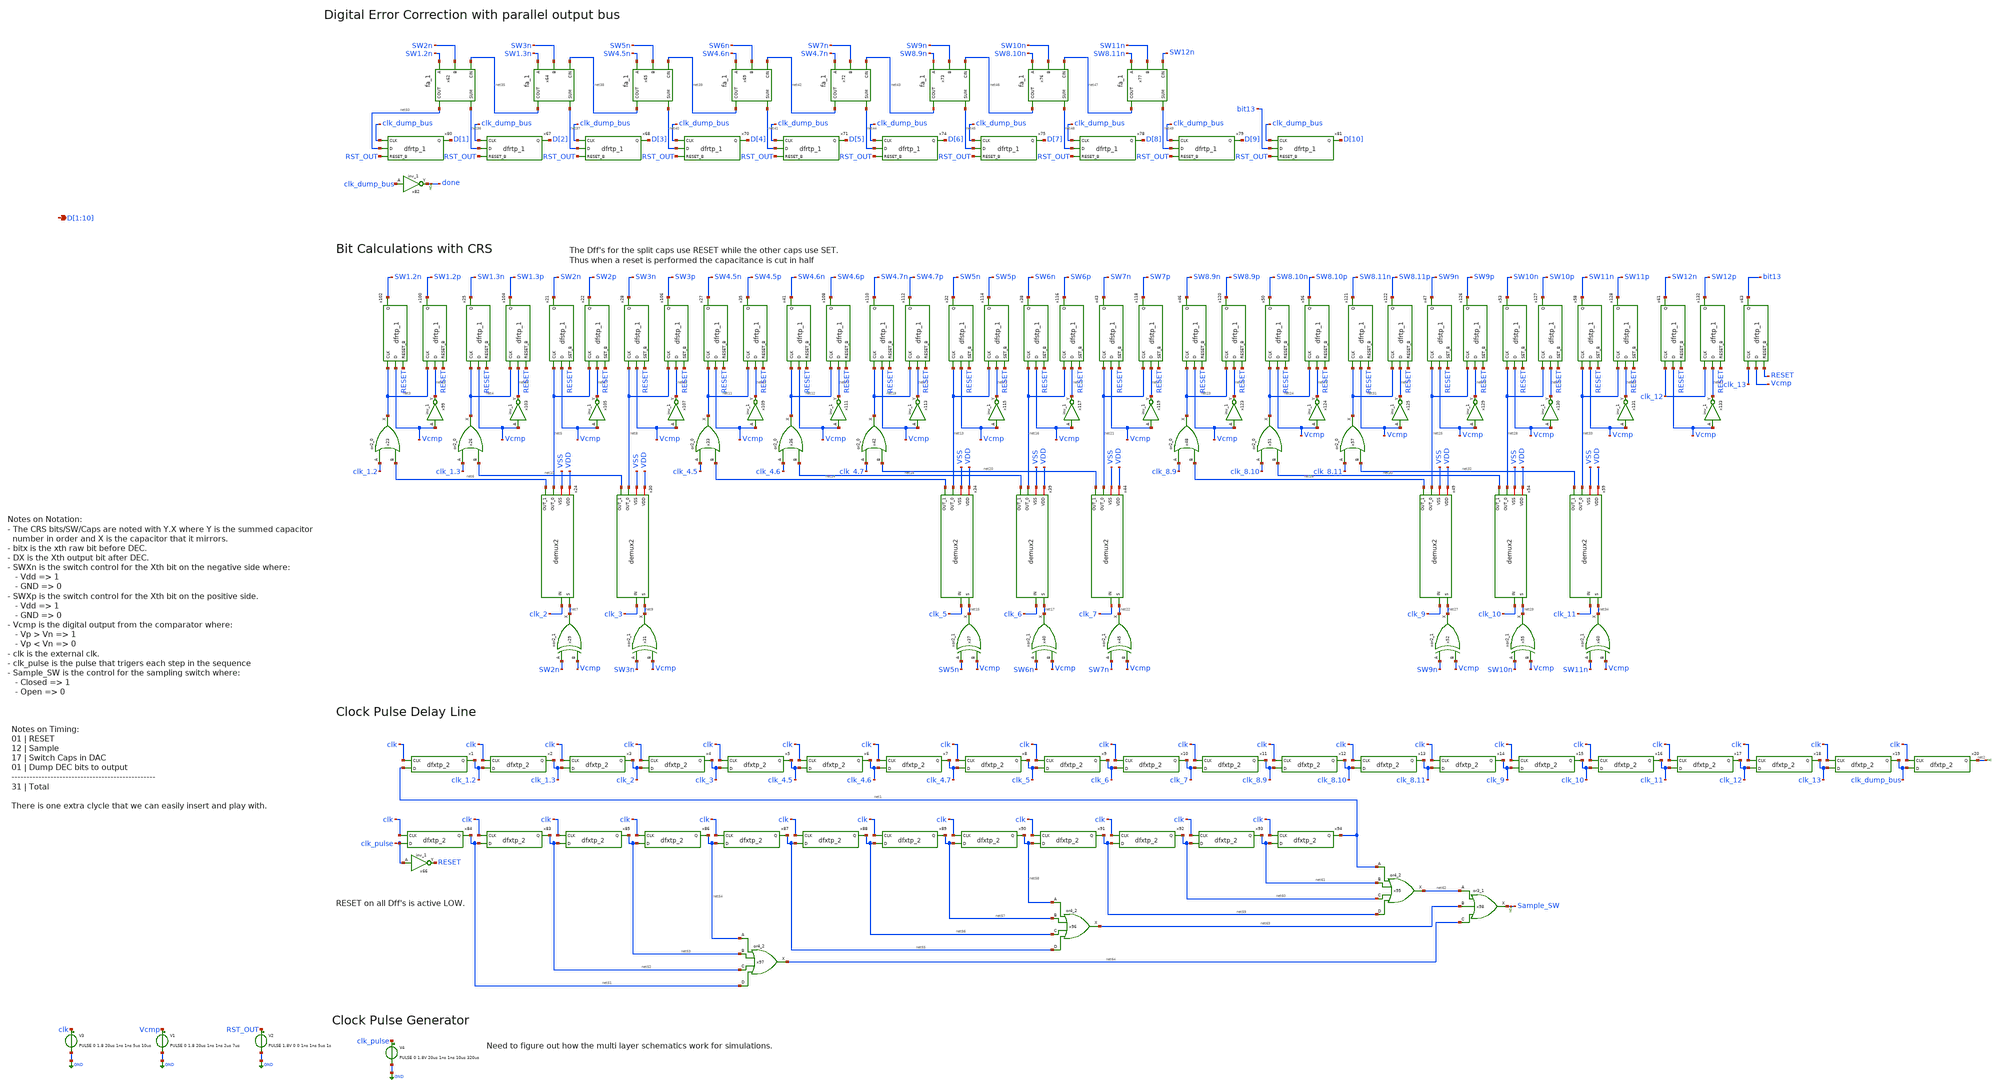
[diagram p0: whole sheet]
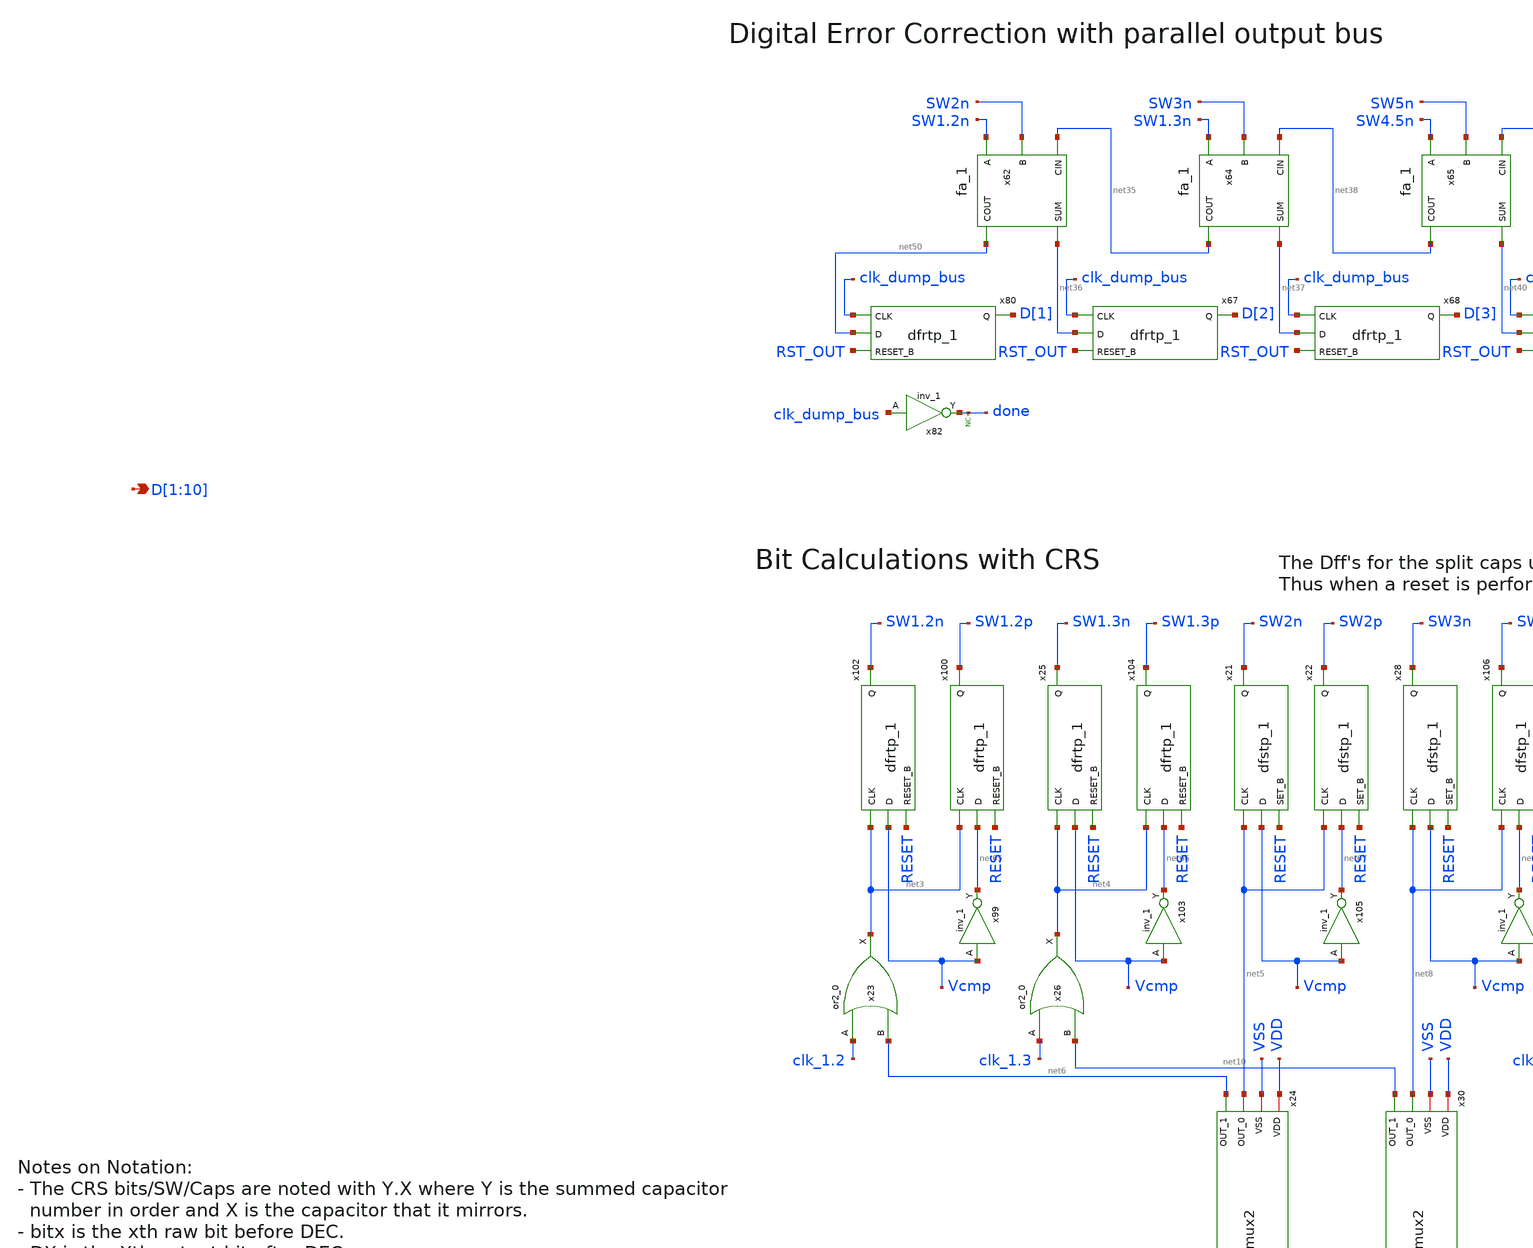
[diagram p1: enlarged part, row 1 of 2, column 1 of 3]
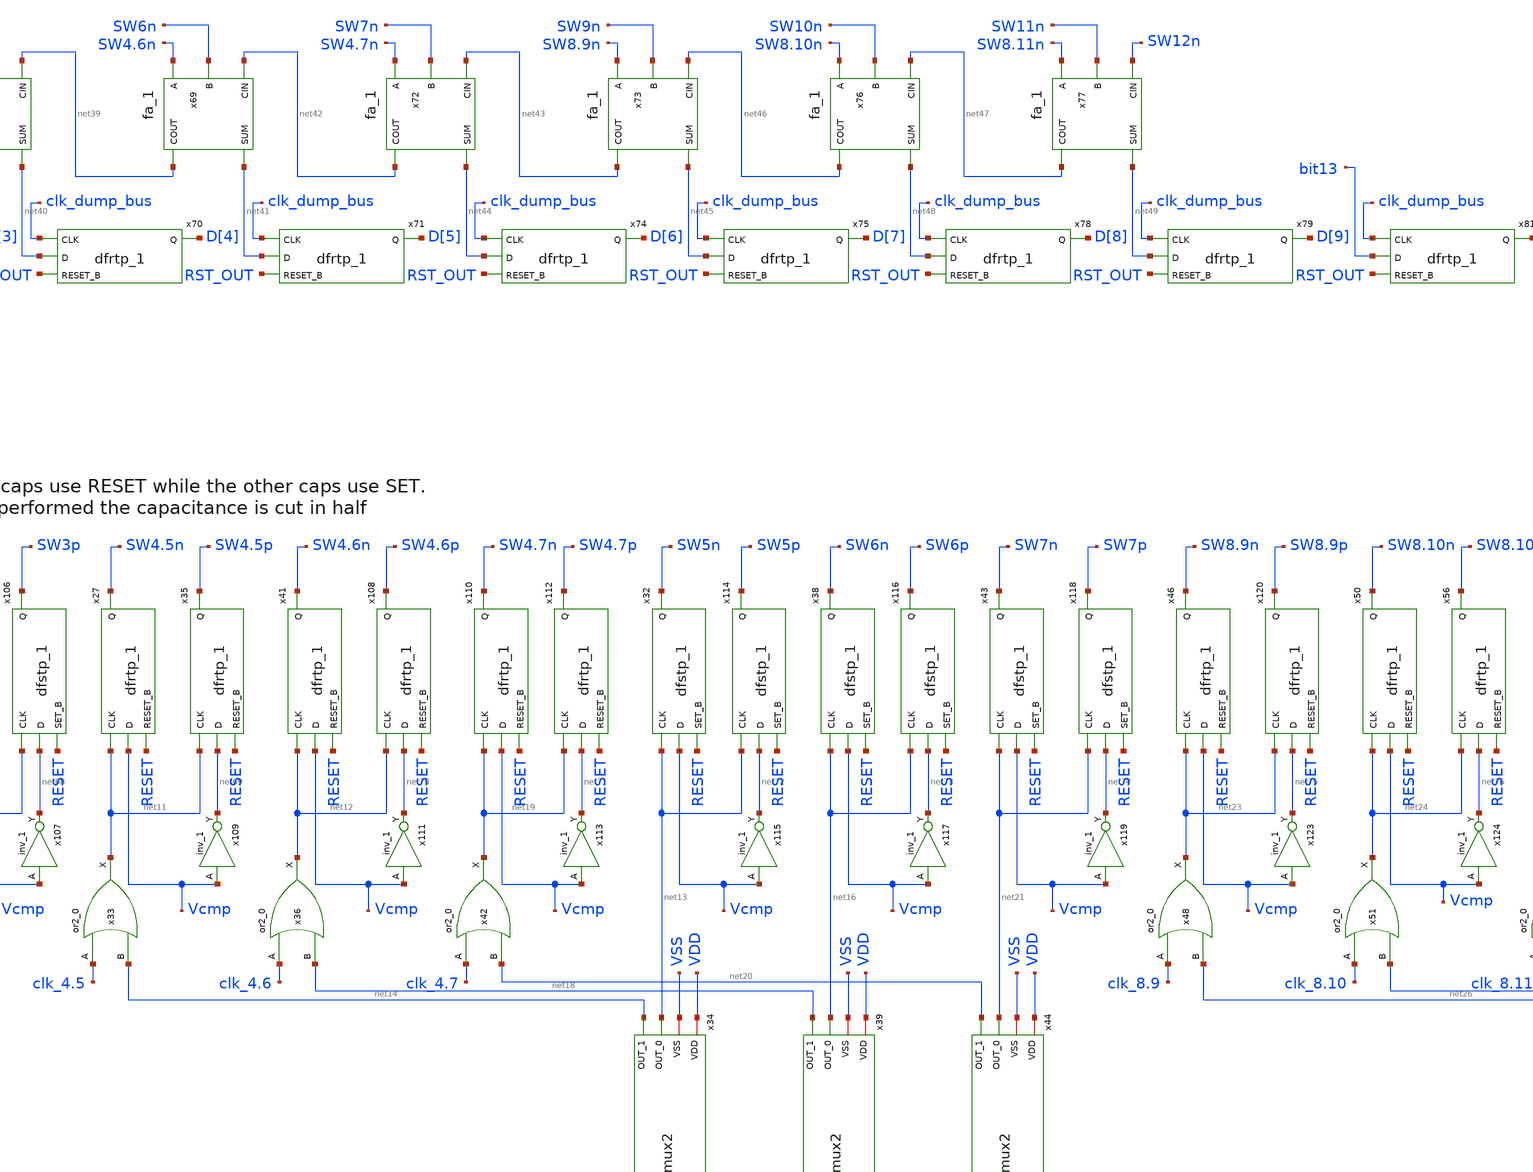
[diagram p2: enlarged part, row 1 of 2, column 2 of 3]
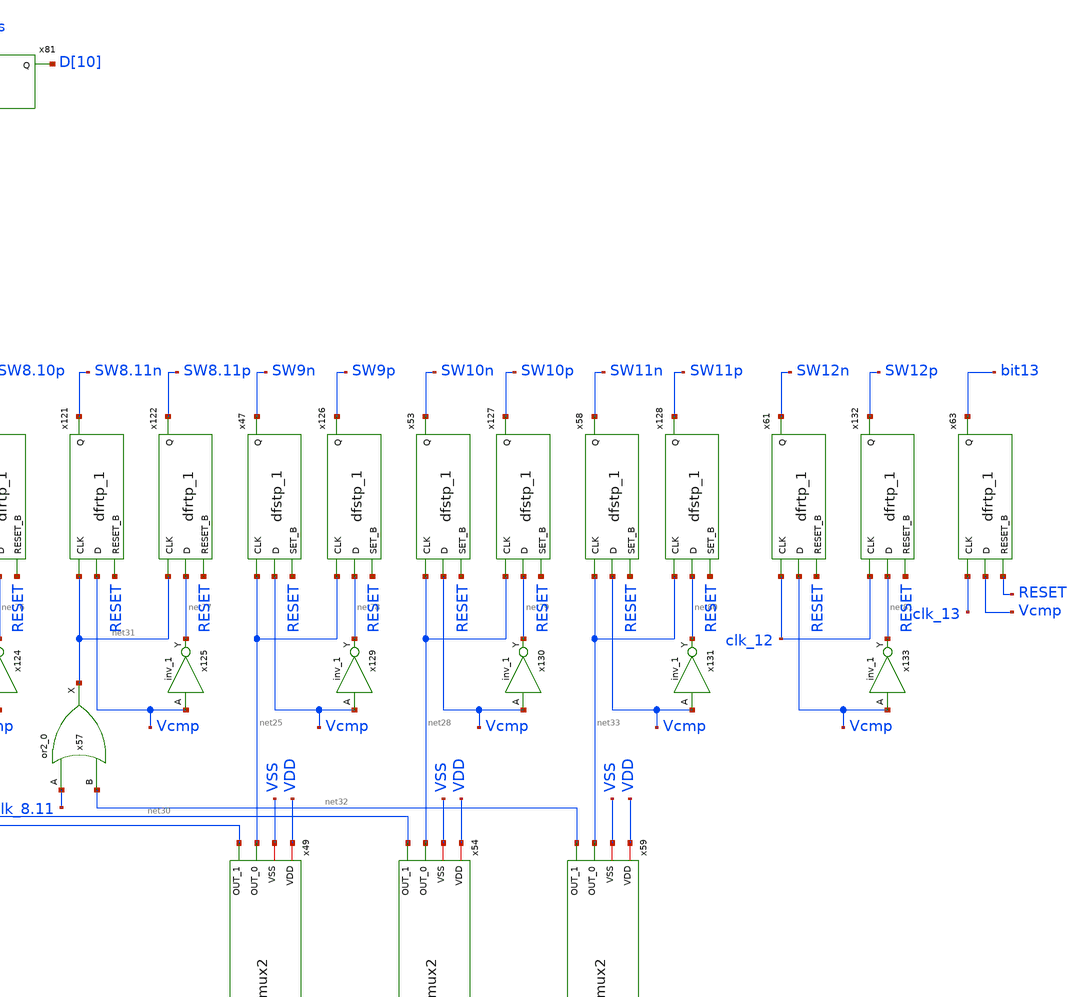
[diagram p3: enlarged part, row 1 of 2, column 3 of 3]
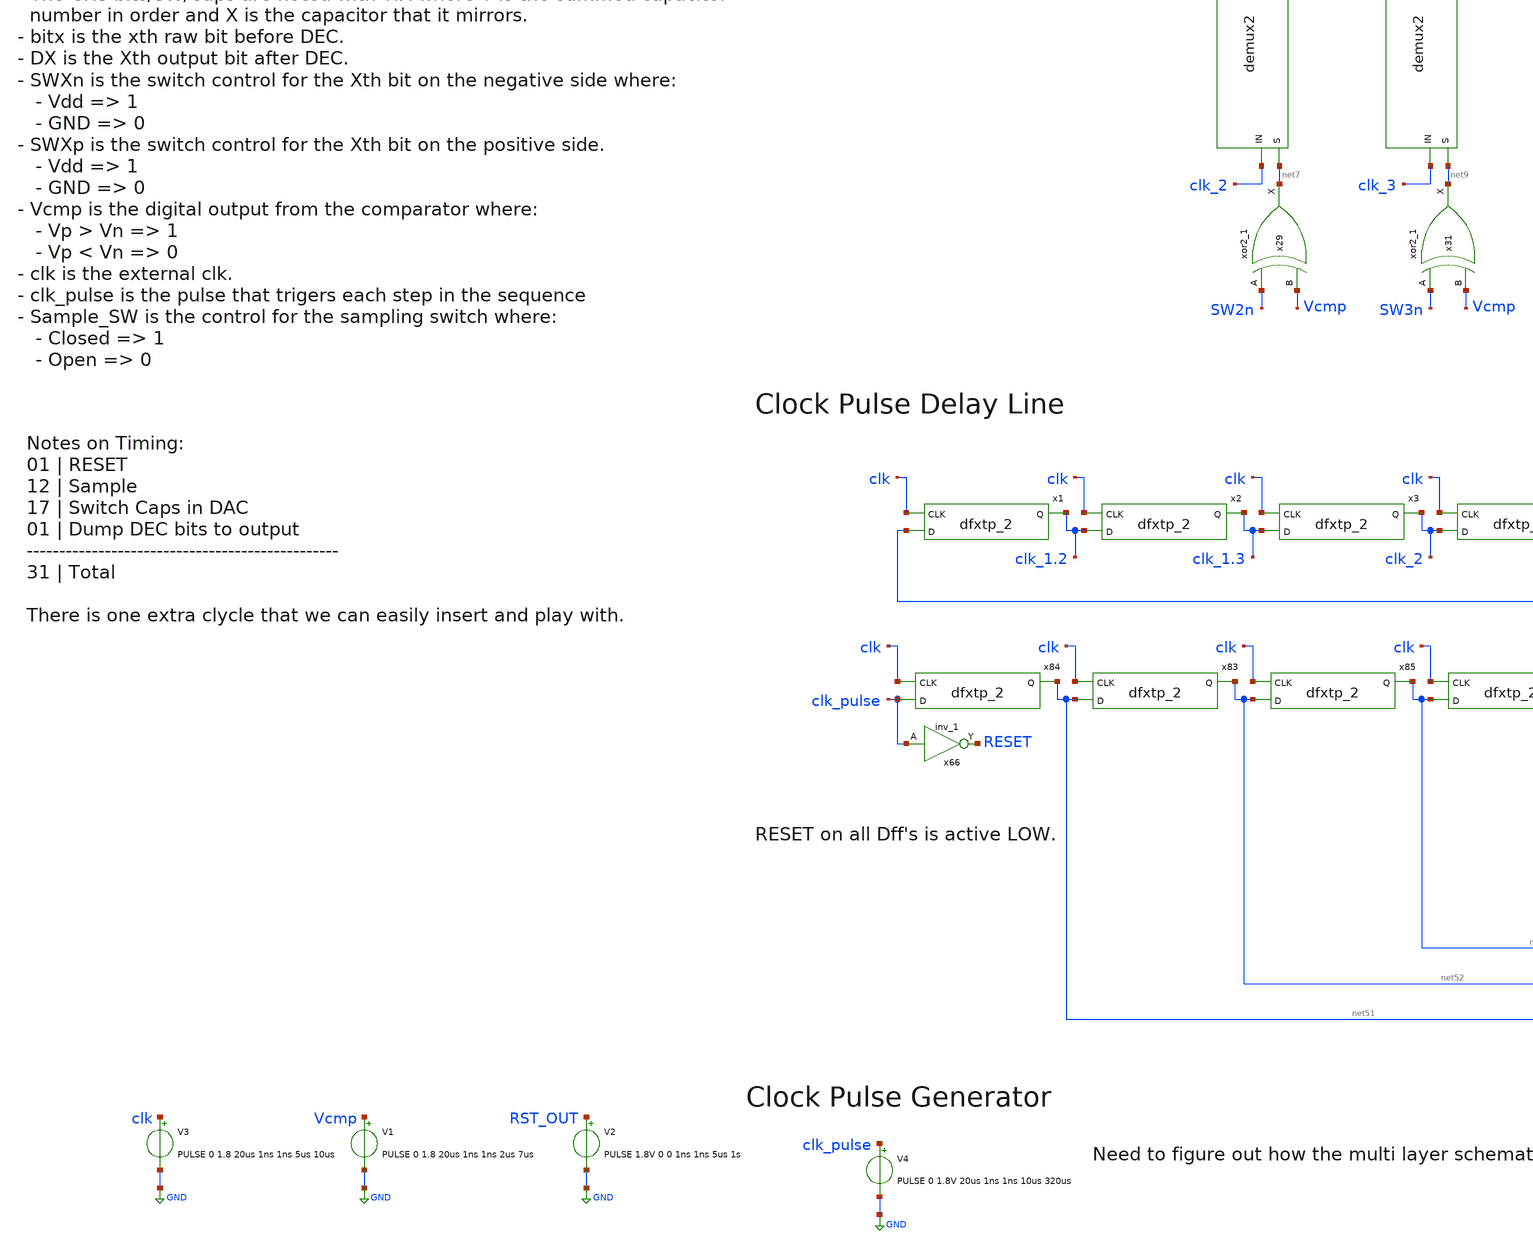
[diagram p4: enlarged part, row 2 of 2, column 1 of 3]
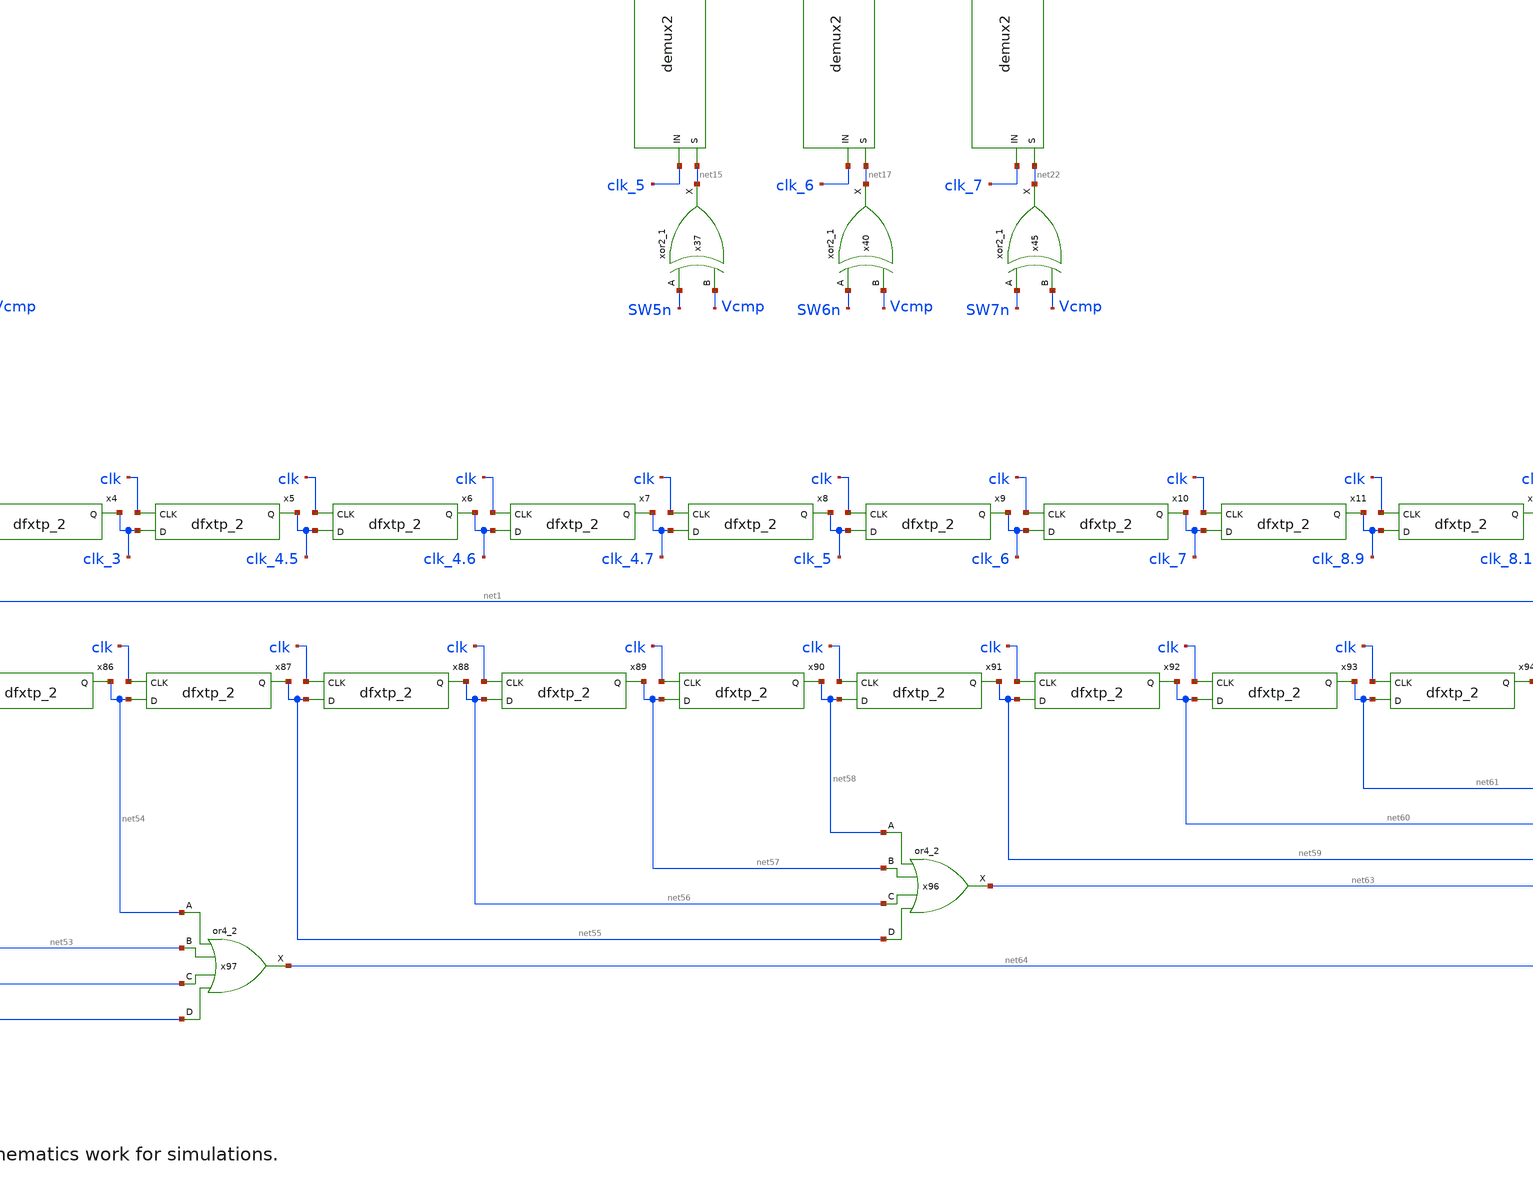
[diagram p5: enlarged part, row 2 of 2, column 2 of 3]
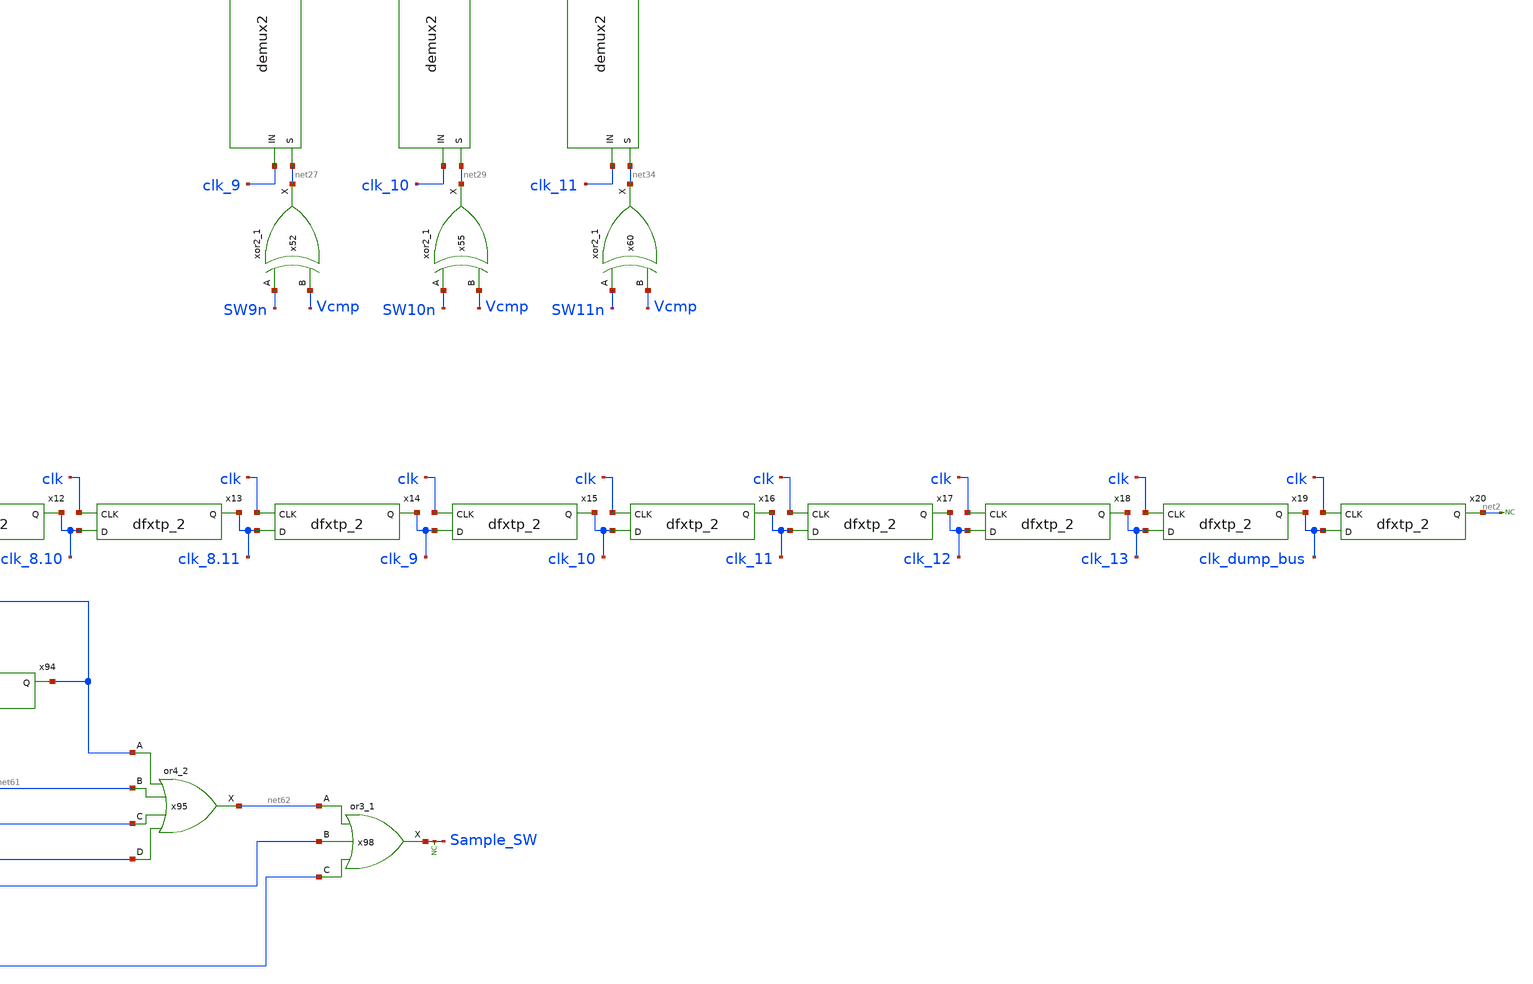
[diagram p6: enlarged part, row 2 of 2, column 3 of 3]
** sch_path: xschem/src/controller/controller.sch
**.subckt controller D[1],D[2],D[3],D[4],D[5],D[6],D[7],D[8],D[9],D[10]
*.opin D[1],D[2],D[3],D[4],D[5],D[6],D[7],D[8],D[9],D[10]
x2 clk clk_1.2 VSS VSS VDD VDD clk_1.3 sky130_fd_sc_hd__dfxtp_2
x1 clk net1 VSS VSS VDD VDD clk_1.2 sky130_fd_sc_hd__dfxtp_2
x3 clk clk_1.3 VSS VSS VDD VDD clk_2 sky130_fd_sc_hd__dfxtp_2
x4 clk clk_2 VSS VSS VDD VDD clk_3 sky130_fd_sc_hd__dfxtp_2
x5 clk clk_3 VSS VSS VDD VDD clk_4.5 sky130_fd_sc_hd__dfxtp_2
x6 clk clk_4.5 VSS VSS VDD VDD clk_4.6 sky130_fd_sc_hd__dfxtp_2
x7 clk clk_4.6 VSS VSS VDD VDD clk_4.7 sky130_fd_sc_hd__dfxtp_2
x8 clk clk_4.7 VSS VSS VDD VDD clk_5 sky130_fd_sc_hd__dfxtp_2
x9 clk clk_5 VSS VSS VDD VDD clk_6 sky130_fd_sc_hd__dfxtp_2
x10 clk clk_6 VSS VSS VDD VDD clk_7 sky130_fd_sc_hd__dfxtp_2
x11 clk clk_7 VSS VSS VDD VDD clk_8.9 sky130_fd_sc_hd__dfxtp_2
x12 clk clk_8.9 VSS VSS VDD VDD clk_8.10 sky130_fd_sc_hd__dfxtp_2
x13 clk clk_8.10 VSS VSS VDD VDD clk_8.11 sky130_fd_sc_hd__dfxtp_2
x14 clk clk_8.11 VSS VSS VDD VDD clk_9 sky130_fd_sc_hd__dfxtp_2
x15 clk clk_9 VSS VSS VDD VDD clk_10 sky130_fd_sc_hd__dfxtp_2
x16 clk clk_10 VSS VSS VDD VDD clk_11 sky130_fd_sc_hd__dfxtp_2
x17 clk clk_11 VSS VSS VDD VDD clk_12 sky130_fd_sc_hd__dfxtp_2
x18 clk clk_12 VSS VSS VDD VDD clk_13 sky130_fd_sc_hd__dfxtp_2
x19 clk clk_13 VSS VSS VDD VDD clk_dump_bus sky130_fd_sc_hd__dfxtp_2
x20 clk clk_dump_bus VSS VSS VDD VDD net2 sky130_fd_sc_hd__dfxtp_2
x23 clk_1.2 net6 VSS VSS VDD VDD net3 sky130_fd_sc_hd__or2_0
x26 clk_1.3 net10 VSS VSS VDD VDD net4 sky130_fd_sc_hd__or2_0
x29 SW2n Vcmp VSS VSS VDD VDD net7 sky130_fd_sc_hd__xor2_1
x31 SW3n Vcmp VSS VSS VDD VDD net9 sky130_fd_sc_hd__xor2_1
x33 clk_4.5 net14 VSS VSS VDD VDD net11 sky130_fd_sc_hd__or2_0
x36 clk_4.6 net18 VSS VSS VDD VDD net12 sky130_fd_sc_hd__or2_0
x37 SW5n Vcmp VSS VSS VDD VDD net15 sky130_fd_sc_hd__xor2_1
x40 SW6n Vcmp VSS VSS VDD VDD net17 sky130_fd_sc_hd__xor2_1
x42 clk_4.7 net20 VSS VSS VDD VDD net19 sky130_fd_sc_hd__or2_0
x45 SW7n Vcmp VSS VSS VDD VDD net22 sky130_fd_sc_hd__xor2_1
x48 clk_8.9 net26 VSS VSS VDD VDD net23 sky130_fd_sc_hd__or2_0
x51 clk_8.10 net30 VSS VSS VDD VDD net24 sky130_fd_sc_hd__or2_0
x52 SW9n Vcmp VSS VSS VDD VDD net27 sky130_fd_sc_hd__xor2_1
x55 SW10n Vcmp VSS VSS VDD VDD net29 sky130_fd_sc_hd__xor2_1
x57 clk_8.11 net32 VSS VSS VDD VDD net31 sky130_fd_sc_hd__or2_0
x60 SW11n Vcmp VSS VSS VDD VDD net34 sky130_fd_sc_hd__xor2_1
x63 clk_13 Vcmp RESET VSS VSS VDD VDD bit13 sky130_fd_sc_hd__dfrtp_1
x62 SW1.2n SW2n net35 VSS VSS VDD VDD net50 net36 sky130_fd_sc_hd__fa_1
x64 SW1.3n SW3n net38 VSS VSS VDD VDD net35 net37 sky130_fd_sc_hd__fa_1
x67 clk_dump_bus net36 RST_OUT VSS VSS VDD VDD D[2] sky130_fd_sc_hd__dfrtp_1
x68 clk_dump_bus net37 RST_OUT VSS VSS VDD VDD D[3] sky130_fd_sc_hd__dfrtp_1
x65 SW4.5n SW5n net39 VSS VSS VDD VDD net38 net40 sky130_fd_sc_hd__fa_1
x69 SW4.6n SW6n net42 VSS VSS VDD VDD net39 net41 sky130_fd_sc_hd__fa_1
x70 clk_dump_bus net40 RST_OUT VSS VSS VDD VDD D[4] sky130_fd_sc_hd__dfrtp_1
x71 clk_dump_bus net41 RST_OUT VSS VSS VDD VDD D[5] sky130_fd_sc_hd__dfrtp_1
x72 SW4.7n SW7n net43 VSS VSS VDD VDD net42 net44 sky130_fd_sc_hd__fa_1
x73 SW8.9n SW9n net46 VSS VSS VDD VDD net43 net45 sky130_fd_sc_hd__fa_1
x74 clk_dump_bus net44 RST_OUT VSS VSS VDD VDD D[6] sky130_fd_sc_hd__dfrtp_1
x75 clk_dump_bus net45 RST_OUT VSS VSS VDD VDD D[7] sky130_fd_sc_hd__dfrtp_1
x76 SW8.10n SW10n net47 VSS VSS VDD VDD net46 net48 sky130_fd_sc_hd__fa_1
x77 SW8.11n SW11n SW12n VSS VSS VDD VDD net47 net49 sky130_fd_sc_hd__fa_1
x78 clk_dump_bus net48 RST_OUT VSS VSS VDD VDD D[8] sky130_fd_sc_hd__dfrtp_1
x79 clk_dump_bus net49 RST_OUT VSS VSS VDD VDD D[9] sky130_fd_sc_hd__dfrtp_1
x80 clk_dump_bus net50 RST_OUT VSS VSS VDD VDD D[1] sky130_fd_sc_hd__dfrtp_1
x81 clk_dump_bus bit13 RST_OUT VSS VSS VDD VDD D[10] sky130_fd_sc_hd__dfrtp_1
x82 clk_dump_bus VSS VSS VDD VDD done sky130_fd_sc_hd__inv_1
x83 clk net51 VSS VSS VDD VDD net52 sky130_fd_sc_hd__dfxtp_2
x84 clk clk_pulse VSS VSS VDD VDD net51 sky130_fd_sc_hd__dfxtp_2
x85 clk net52 VSS VSS VDD VDD net53 sky130_fd_sc_hd__dfxtp_2
x86 clk net53 VSS VSS VDD VDD net54 sky130_fd_sc_hd__dfxtp_2
x87 clk net54 VSS VSS VDD VDD net55 sky130_fd_sc_hd__dfxtp_2
x88 clk net55 VSS VSS VDD VDD net56 sky130_fd_sc_hd__dfxtp_2
x89 clk net56 VSS VSS VDD VDD net57 sky130_fd_sc_hd__dfxtp_2
x90 clk net57 VSS VSS VDD VDD net58 sky130_fd_sc_hd__dfxtp_2
x91 clk net58 VSS VSS VDD VDD net59 sky130_fd_sc_hd__dfxtp_2
x92 clk net59 VSS VSS VDD VDD net60 sky130_fd_sc_hd__dfxtp_2
x93 clk net60 VSS VSS VDD VDD net61 sky130_fd_sc_hd__dfxtp_2
x94 clk net61 VSS VSS VDD VDD net1 sky130_fd_sc_hd__dfxtp_2
x66 clk_pulse VSS VSS VDD VDD RESET sky130_fd_sc_hd__inv_1
x95 net1 net61 net60 net59 VSS VSS VDD VDD net62 sky130_fd_sc_hd__or4_2
x96 net58 net57 net56 net55 VSS VSS VDD VDD net63 sky130_fd_sc_hd__or4_2
x97 net54 net53 net52 net51 VSS VSS VDD VDD net64 sky130_fd_sc_hd__or4_2
x98 net62 net63 net64 VSS VSS VDD VDD Sample_SW sky130_fd_sc_hd__or3_1
V1 Vcmp GND PULSE 0 1.8 20us 1ns 1ns 2us 7us
V2 RST_OUT GND PULSE 1.8V 0 0 1ns 1ns 5us 1s
* noconn #net2
* noconn Sample_SW
* noconn done
V3 clk GND PULSE 0 1.8 20us 1ns 1ns 5us 10us
V4 clk_pulse GND PULSE 0 1.8V 20us 1ns 1ns 10us 320us
x100 net3 net65 RESET VSS VSS VDD VDD SW1.2p sky130_fd_sc_hd__dfrtp_1
x99 Vcmp VSS VSS VDD VDD net65 sky130_fd_sc_hd__inv_1
x102 net3 Vcmp RESET VSS VSS VDD VDD SW1.2n sky130_fd_sc_hd__dfrtp_1
x25 net4 Vcmp RESET VSS VSS VDD VDD SW1.3n sky130_fd_sc_hd__dfrtp_1
x103 Vcmp VSS VSS VDD VDD net66 sky130_fd_sc_hd__inv_1
x104 net4 net66 RESET VSS VSS VDD VDD SW1.3p sky130_fd_sc_hd__dfrtp_1
x21 net5 Vcmp RESET VSS VSS VDD VDD SW2n sky130_fd_sc_hd__dfstp_1
x22 net5 net67 RESET VSS VSS VDD VDD SW2p sky130_fd_sc_hd__dfstp_1
x105 Vcmp VSS VSS VDD VDD net67 sky130_fd_sc_hd__inv_1
x28 net8 Vcmp RESET VSS VSS VDD VDD SW3n sky130_fd_sc_hd__dfstp_1
x106 net8 net68 RESET VSS VSS VDD VDD SW3p sky130_fd_sc_hd__dfstp_1
x107 Vcmp VSS VSS VDD VDD net68 sky130_fd_sc_hd__inv_1
x109 Vcmp VSS VSS VDD VDD net69 sky130_fd_sc_hd__inv_1
x111 Vcmp VSS VSS VDD VDD net70 sky130_fd_sc_hd__inv_1
x27 net11 Vcmp RESET VSS VSS VDD VDD SW4.5n sky130_fd_sc_hd__dfrtp_1
x35 net11 net69 RESET VSS VSS VDD VDD SW4.5p sky130_fd_sc_hd__dfrtp_1
x41 net12 Vcmp RESET VSS VSS VDD VDD SW4.6n sky130_fd_sc_hd__dfrtp_1
x108 net12 net70 RESET VSS VSS VDD VDD SW4.6p sky130_fd_sc_hd__dfrtp_1
x110 net19 Vcmp RESET VSS VSS VDD VDD SW4.7n sky130_fd_sc_hd__dfrtp_1
x112 net19 net71 RESET VSS VSS VDD VDD SW4.7p sky130_fd_sc_hd__dfrtp_1
x113 Vcmp VSS VSS VDD VDD net71 sky130_fd_sc_hd__inv_1
x114 net13 net72 RESET VSS VSS VDD VDD SW5p sky130_fd_sc_hd__dfstp_1
x32 net13 Vcmp RESET VSS VSS VDD VDD SW5n sky130_fd_sc_hd__dfstp_1
x115 Vcmp VSS VSS VDD VDD net72 sky130_fd_sc_hd__inv_1
x38 net16 Vcmp RESET VSS VSS VDD VDD SW6n sky130_fd_sc_hd__dfstp_1
x116 net16 net73 RESET VSS VSS VDD VDD SW6p sky130_fd_sc_hd__dfstp_1
x117 Vcmp VSS VSS VDD VDD net73 sky130_fd_sc_hd__inv_1
x43 net21 Vcmp RESET VSS VSS VDD VDD SW7n sky130_fd_sc_hd__dfstp_1
x118 net21 net74 RESET VSS VSS VDD VDD SW7p sky130_fd_sc_hd__dfstp_1
x119 Vcmp VSS VSS VDD VDD net74 sky130_fd_sc_hd__inv_1
x120 net23 net75 RESET VSS VSS VDD VDD SW8.9p sky130_fd_sc_hd__dfrtp_1
x46 net23 Vcmp RESET VSS VSS VDD VDD SW8.9n sky130_fd_sc_hd__dfrtp_1
x50 net24 Vcmp RESET VSS VSS VDD VDD SW8.10n sky130_fd_sc_hd__dfrtp_1
x56 net24 net76 RESET VSS VSS VDD VDD SW8.10p sky130_fd_sc_hd__dfrtp_1
x121 net31 Vcmp RESET VSS VSS VDD VDD SW8.11n sky130_fd_sc_hd__dfrtp_1
x122 net31 net77 RESET VSS VSS VDD VDD SW8.11p sky130_fd_sc_hd__dfrtp_1
x123 Vcmp VSS VSS VDD VDD net75 sky130_fd_sc_hd__inv_1
x124 Vcmp VSS VSS VDD VDD net76 sky130_fd_sc_hd__inv_1
x125 Vcmp VSS VSS VDD VDD net77 sky130_fd_sc_hd__inv_1
x126 net25 net78 RESET VSS VSS VDD VDD SW9p sky130_fd_sc_hd__dfstp_1
x47 net25 Vcmp RESET VSS VSS VDD VDD SW9n sky130_fd_sc_hd__dfstp_1
x53 net28 Vcmp RESET VSS VSS VDD VDD SW10n sky130_fd_sc_hd__dfstp_1
x58 net33 Vcmp RESET VSS VSS VDD VDD SW11n sky130_fd_sc_hd__dfstp_1
x127 net28 net79 RESET VSS VSS VDD VDD SW10p sky130_fd_sc_hd__dfstp_1
x128 net33 net80 RESET VSS VSS VDD VDD SW11p sky130_fd_sc_hd__dfstp_1
x129 Vcmp VSS VSS VDD VDD net78 sky130_fd_sc_hd__inv_1
x130 Vcmp VSS VSS VDD VDD net79 sky130_fd_sc_hd__inv_1
x131 Vcmp VSS VSS VDD VDD net80 sky130_fd_sc_hd__inv_1
x132 clk_12 net81 RESET VSS VSS VDD VDD SW12p sky130_fd_sc_hd__dfrtp_1
x133 Vcmp VSS VSS VDD VDD net81 sky130_fd_sc_hd__inv_1
x61 clk_12 Vcmp RESET VSS VSS VDD VDD SW12n sky130_fd_sc_hd__dfrtp_1
x24 net7 VDD VSS net5 clk_2 net6 demux2
x30 net9 VDD VSS net8 clk_3 net10 demux2
x34 net15 VDD VSS net13 clk_5 net14 demux2
x39 net17 VDD VSS net16 clk_6 net18 demux2
x44 net22 VDD VSS net21 clk_7 net20 demux2
x49 net27 VDD VSS net25 clk_9 net26 demux2
x54 net29 VDD VSS net28 clk_10 net30 demux2
x59 net34 VDD VSS net33 clk_11 net32 demux2
**** begin user architecture code
 .lib $::SKYWATER_MODELS/sky130.lib.spice tt
.include $::SKYWATER_STDCELLS/sky130_fd_sc_hd.spice



.options acct list
.temp 25
vvcc VDD 0 dc 1.8
vvss VSS 0 0
.control
tran 0.1u 400u
* plot a b+2 clk+4 reset_b+6 x+8 y+10 q+12 qlatch+14
plot RST_OUT-2 clk Vcmp+2
plot D[1] D[2]+2 D[3]+4 D[4]+6 D[5]+8 D[6]+10 D[7]+12 D[8]+14 D[9]+16 D[10]+18
write controller.raw
.endc


**** end user architecture code
**.ends

* expanding   symbol:  src/demux2/demux2.sym # of pins=6
** sym_path: xschem/src/demux2/demux2.sym
** sch_path: xschem/src/demux2/demux2.sch
.subckt demux2 S VDD VSS OUT_0 IN OUT_1
*.ipin S
*.opin OUT_0
*.ipin IN
*.opin OUT_1
*.iopin VDD
*.iopin VSS
x1 net1 IN VSS VSS VDD VDD OUT_0 sky130_fd_sc_hd__and2_0
x2 S IN VSS VSS VDD VDD OUT_1 sky130_fd_sc_hd__and2_0
x3 S VSS VSS VDD VDD net1 sky130_fd_sc_hd__inv_1
.ends

.GLOBAL GND
.end
